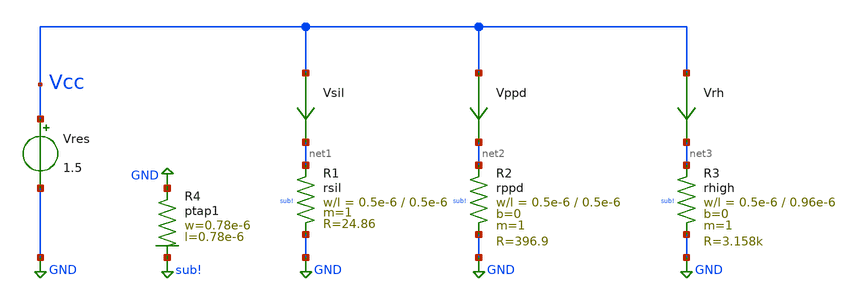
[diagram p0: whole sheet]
** sch_path: ihp-sg13g2/xschem_libs/sg13g2_tests_ase/dc_res_temp/schematic/dc_res_temp.sch
* Copyright 2023 IHP PDK Authors
**.subckt dc_res_temp
Vres Vcc GND 1.5
Vsil Vcc net1 0
.save i(vsil)
Vppd Vcc net2 0
.save i(vppd)
Vrh Vcc net3 0
.save i(vrh)
XR4 GND sub! ptap1 R=262.8 w=0.78e-6 l=0.78e-6
XR1 net1 GND sub! rsil w=0.5e-6 l=0.5e-6 m=1 mm_ok=1
XR3 net3 GND sub! rhigh w=0.5e-6 l=0.96e-6 m=1 b=0 mm_ok=1
XR2 net2 GND sub! rppd w=0.5e-6 l=0.5e-6 m=1 b=0 mm_ok=1
**.ends
.GLOBAL GND
.GLOBAL sub!
.end
